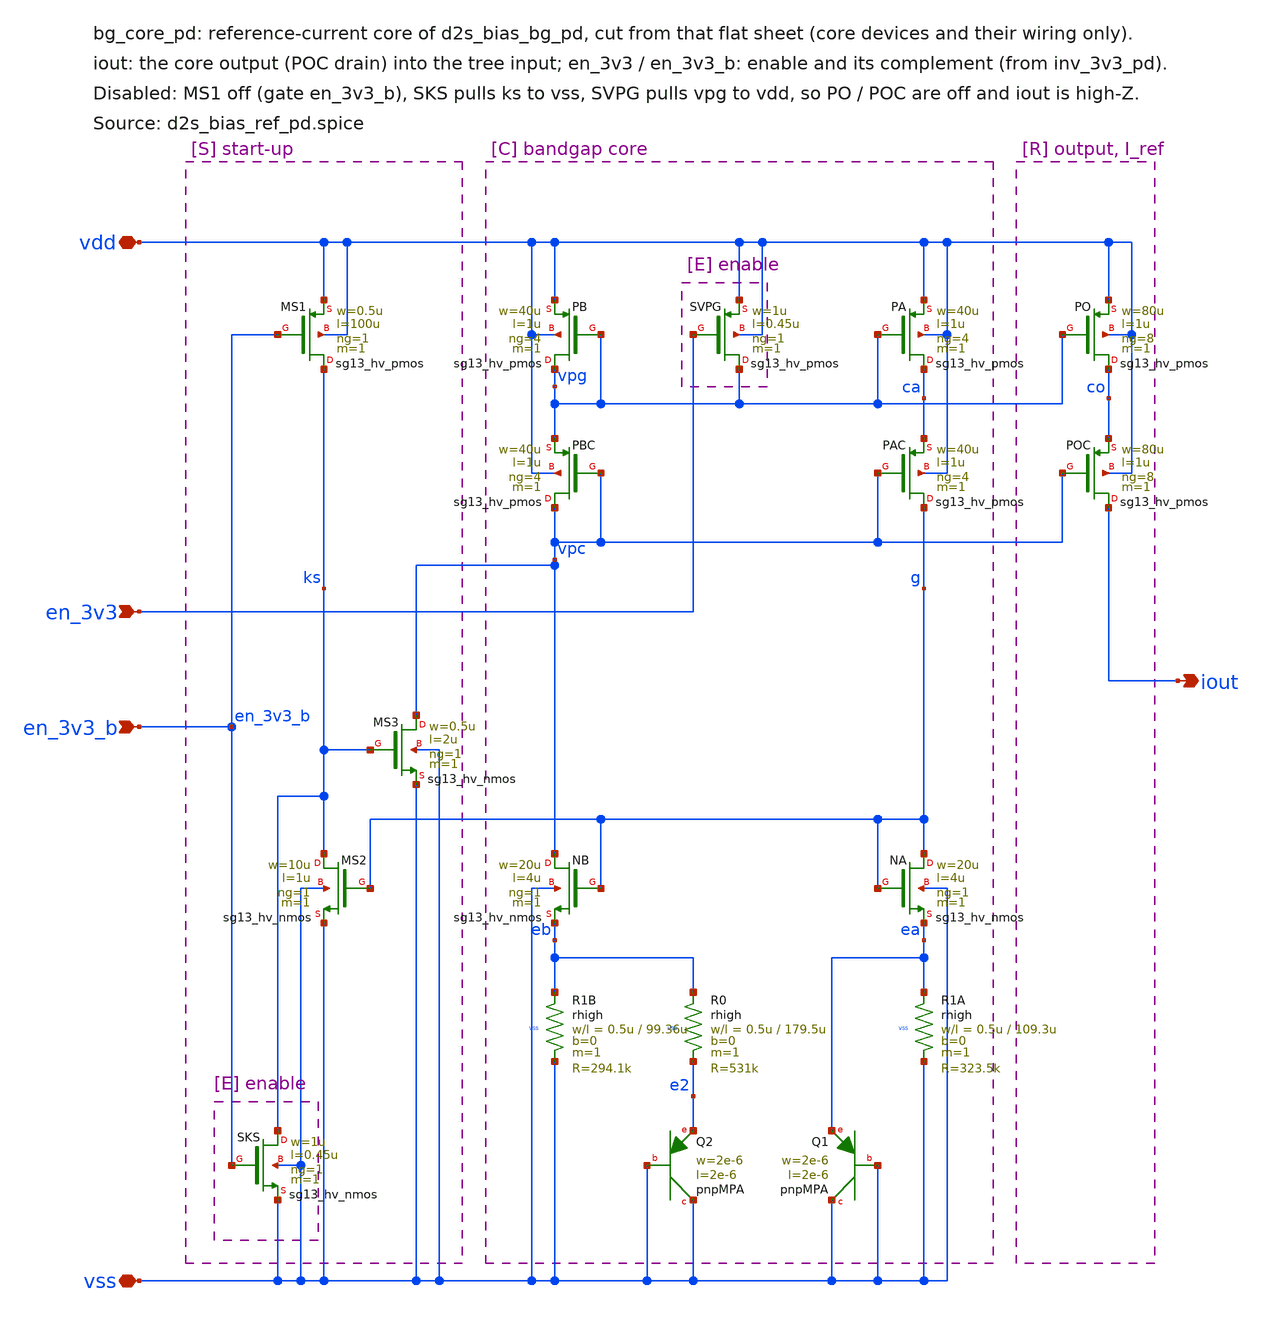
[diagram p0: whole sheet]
** sch_path: sudelbuecher/design_considerations/consolidation/bias_hierarchy_2026-10-27/before/macros/d2s_bias_sel_pd/schematic/xschem/bg_core_pd.sch
**.subckt bg_core_pd vdd vss en_3v3 en_3v3_b iout
*.iopin vdd
*.iopin vss
*.ipin en_3v3
*.ipin en_3v3_b
*.opin iout
XMS1 ks en_3v3_b vdd vdd sg13_hv_pmos w=0.5u l=100u ng=1 m=1 mm_ok=1
XMS2 ks g vss vss sg13_hv_nmos w=10u l=1u ng=1 m=1 mm_ok=1
XMS3 vpc ks vss vss sg13_hv_nmos w=0.5u l=2u ng=1 m=1 mm_ok=1
XPB vpg vpg vdd vdd sg13_hv_pmos w=40u l=1u ng=4 m=1 mm_ok=1
XPBC vpc vpc vpg vdd sg13_hv_pmos w=40u l=1u ng=4 m=1 mm_ok=1
XNB vpc g eb vss sg13_hv_nmos w=20u l=4u ng=1 m=1 mm_ok=1
XR1B eb vss vss rhigh w=0.5u l=99.36u m=1 b=0 mm_ok=1
XR0 eb e2 vss rhigh w=0.5u l=179.5u m=1 b=0 mm_ok=1
XQ2 vss vss e2 pnpMPA a=4p p=8u m=8
XPA ca vpg vdd vdd sg13_hv_pmos w=40u l=1u ng=4 m=1 mm_ok=1
XPAC g vpc ca vdd sg13_hv_pmos w=40u l=1u ng=4 m=1 mm_ok=1
XNA g g ea vss sg13_hv_nmos w=20u l=4u ng=1 m=1 mm_ok=1
XR1A ea vss vss rhigh w=0.5u l=109.3u m=1 b=0 mm_ok=1
XQ1 vss vss ea pnpMPA a=4p p=8u m=1
XPO co vpg vdd vdd sg13_hv_pmos w=80u l=1u ng=8 m=1 mm_ok=1
XPOC iout vpc co vdd sg13_hv_pmos w=80u l=1u ng=8 m=1 mm_ok=1
XSKS ks en_3v3_b vss vss sg13_hv_nmos w=1u l=0.45u ng=1 m=1 mm_ok=1
XSVPG vpg en_3v3 vdd vdd sg13_hv_pmos w=1u l=0.45u ng=1 m=1 mm_ok=1
**.ends
.end
